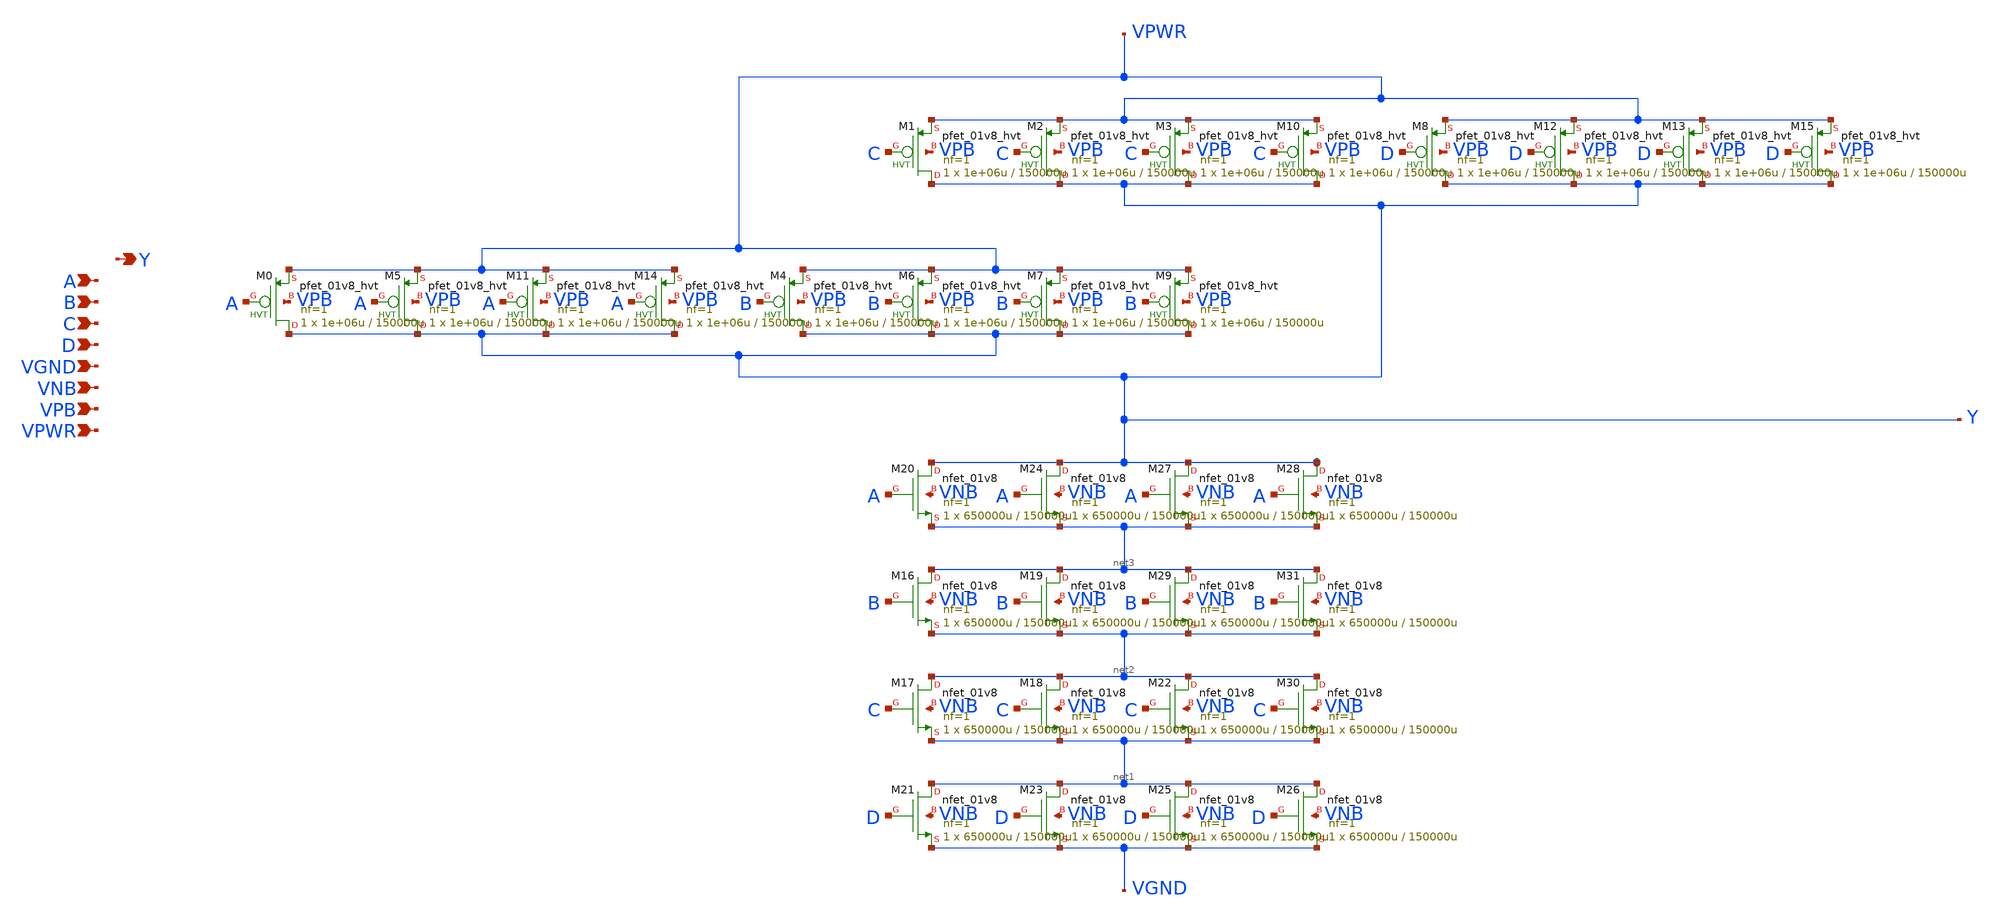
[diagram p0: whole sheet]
** sch_path: schematics/nand4/sky130_fd_sc_hd__nand4_4.sch
**.subckt sky130_fd_sc_hd__nand4_4 A B C D VGND VNB VPB VPWR Y
*.ipin A
*.ipin B
*.ipin C
*.ipin D
*.ipin VGND
*.ipin VNB
*.ipin VPB
*.ipin VPWR
*.opin Y
XM0 Y A VPWR VPB sky130_fd_pr__pfet_01v8_hvt L=150000u W=1e+06u nf=1 ad='int((1 + 1)/2) * 1e+06u / 1 * 0.29'
+ as='int((1 + 2)/2) * 1e+06u / 1 * 0.29' pd='2*int((1 + 1)/2) * (1e+06u / 1 + 0.29)' ps='2*int((1 + 2)/2) * (1e+06u / 1 + 0.29)'
+ nrd='0.29 / 1e+06u ' nrs='0.29 / 1e+06u ' sa=0 sb=0 sd=0 mult=1 m=1
XM1 Y C VPWR VPB sky130_fd_pr__pfet_01v8_hvt L=150000u W=1e+06u nf=1 ad='int((1 + 1)/2) * 1e+06u / 1 * 0.29'
+ as='int((1 + 2)/2) * 1e+06u / 1 * 0.29' pd='2*int((1 + 1)/2) * (1e+06u / 1 + 0.29)' ps='2*int((1 + 2)/2) * (1e+06u / 1 + 0.29)'
+ nrd='0.29 / 1e+06u ' nrs='0.29 / 1e+06u ' sa=0 sb=0 sd=0 mult=1 m=1
XM2 Y C VPWR VPB sky130_fd_pr__pfet_01v8_hvt L=150000u W=1e+06u nf=1 ad='int((1 + 1)/2) * 1e+06u / 1 * 0.29'
+ as='int((1 + 2)/2) * 1e+06u / 1 * 0.29' pd='2*int((1 + 1)/2) * (1e+06u / 1 + 0.29)' ps='2*int((1 + 2)/2) * (1e+06u / 1 + 0.29)'
+ nrd='0.29 / 1e+06u ' nrs='0.29 / 1e+06u ' sa=0 sb=0 sd=0 mult=1 m=1
XM3 Y C VPWR VPB sky130_fd_pr__pfet_01v8_hvt L=150000u W=1e+06u nf=1 ad='int((1 + 1)/2) * 1e+06u / 1 * 0.29'
+ as='int((1 + 2)/2) * 1e+06u / 1 * 0.29' pd='2*int((1 + 1)/2) * (1e+06u / 1 + 0.29)' ps='2*int((1 + 2)/2) * (1e+06u / 1 + 0.29)'
+ nrd='0.29 / 1e+06u ' nrs='0.29 / 1e+06u ' sa=0 sb=0 sd=0 mult=1 m=1
XM4 Y B VPWR VPB sky130_fd_pr__pfet_01v8_hvt L=150000u W=1e+06u nf=1 ad='int((1 + 1)/2) * 1e+06u / 1 * 0.29'
+ as='int((1 + 2)/2) * 1e+06u / 1 * 0.29' pd='2*int((1 + 1)/2) * (1e+06u / 1 + 0.29)' ps='2*int((1 + 2)/2) * (1e+06u / 1 + 0.29)'
+ nrd='0.29 / 1e+06u ' nrs='0.29 / 1e+06u ' sa=0 sb=0 sd=0 mult=1 m=1
XM5 Y A VPWR VPB sky130_fd_pr__pfet_01v8_hvt L=150000u W=1e+06u nf=1 ad='int((1 + 1)/2) * 1e+06u / 1 * 0.29'
+ as='int((1 + 2)/2) * 1e+06u / 1 * 0.29' pd='2*int((1 + 1)/2) * (1e+06u / 1 + 0.29)' ps='2*int((1 + 2)/2) * (1e+06u / 1 + 0.29)'
+ nrd='0.29 / 1e+06u ' nrs='0.29 / 1e+06u ' sa=0 sb=0 sd=0 mult=1 m=1
XM6 Y B VPWR VPB sky130_fd_pr__pfet_01v8_hvt L=150000u W=1e+06u nf=1 ad='int((1 + 1)/2) * 1e+06u / 1 * 0.29'
+ as='int((1 + 2)/2) * 1e+06u / 1 * 0.29' pd='2*int((1 + 1)/2) * (1e+06u / 1 + 0.29)' ps='2*int((1 + 2)/2) * (1e+06u / 1 + 0.29)'
+ nrd='0.29 / 1e+06u ' nrs='0.29 / 1e+06u ' sa=0 sb=0 sd=0 mult=1 m=1
XM7 Y B VPWR VPB sky130_fd_pr__pfet_01v8_hvt L=150000u W=1e+06u nf=1 ad='int((1 + 1)/2) * 1e+06u / 1 * 0.29'
+ as='int((1 + 2)/2) * 1e+06u / 1 * 0.29' pd='2*int((1 + 1)/2) * (1e+06u / 1 + 0.29)' ps='2*int((1 + 2)/2) * (1e+06u / 1 + 0.29)'
+ nrd='0.29 / 1e+06u ' nrs='0.29 / 1e+06u ' sa=0 sb=0 sd=0 mult=1 m=1
XM8 Y D VPWR VPB sky130_fd_pr__pfet_01v8_hvt L=150000u W=1e+06u nf=1 ad='int((1 + 1)/2) * 1e+06u / 1 * 0.29'
+ as='int((1 + 2)/2) * 1e+06u / 1 * 0.29' pd='2*int((1 + 1)/2) * (1e+06u / 1 + 0.29)' ps='2*int((1 + 2)/2) * (1e+06u / 1 + 0.29)'
+ nrd='0.29 / 1e+06u ' nrs='0.29 / 1e+06u ' sa=0 sb=0 sd=0 mult=1 m=1
XM9 Y B VPWR VPB sky130_fd_pr__pfet_01v8_hvt L=150000u W=1e+06u nf=1 ad='int((1 + 1)/2) * 1e+06u / 1 * 0.29'
+ as='int((1 + 2)/2) * 1e+06u / 1 * 0.29' pd='2*int((1 + 1)/2) * (1e+06u / 1 + 0.29)' ps='2*int((1 + 2)/2) * (1e+06u / 1 + 0.29)'
+ nrd='0.29 / 1e+06u ' nrs='0.29 / 1e+06u ' sa=0 sb=0 sd=0 mult=1 m=1
XM10 Y C VPWR VPB sky130_fd_pr__pfet_01v8_hvt L=150000u W=1e+06u nf=1 ad='int((1 + 1)/2) * 1e+06u / 1 * 0.29'
+ as='int((1 + 2)/2) * 1e+06u / 1 * 0.29' pd='2*int((1 + 1)/2) * (1e+06u / 1 + 0.29)' ps='2*int((1 + 2)/2) * (1e+06u / 1 + 0.29)'
+ nrd='0.29 / 1e+06u ' nrs='0.29 / 1e+06u ' sa=0 sb=0 sd=0 mult=1 m=1
XM11 Y A VPWR VPB sky130_fd_pr__pfet_01v8_hvt L=150000u W=1e+06u nf=1 ad='int((1 + 1)/2) * 1e+06u / 1 * 0.29'
+ as='int((1 + 2)/2) * 1e+06u / 1 * 0.29' pd='2*int((1 + 1)/2) * (1e+06u / 1 + 0.29)' ps='2*int((1 + 2)/2) * (1e+06u / 1 + 0.29)'
+ nrd='0.29 / 1e+06u ' nrs='0.29 / 1e+06u ' sa=0 sb=0 sd=0 mult=1 m=1
XM12 Y D VPWR VPB sky130_fd_pr__pfet_01v8_hvt L=150000u W=1e+06u nf=1 ad='int((1 + 1)/2) * 1e+06u / 1 * 0.29'
+ as='int((1 + 2)/2) * 1e+06u / 1 * 0.29' pd='2*int((1 + 1)/2) * (1e+06u / 1 + 0.29)' ps='2*int((1 + 2)/2) * (1e+06u / 1 + 0.29)'
+ nrd='0.29 / 1e+06u ' nrs='0.29 / 1e+06u ' sa=0 sb=0 sd=0 mult=1 m=1
XM13 Y D VPWR VPB sky130_fd_pr__pfet_01v8_hvt L=150000u W=1e+06u nf=1 ad='int((1 + 1)/2) * 1e+06u / 1 * 0.29'
+ as='int((1 + 2)/2) * 1e+06u / 1 * 0.29' pd='2*int((1 + 1)/2) * (1e+06u / 1 + 0.29)' ps='2*int((1 + 2)/2) * (1e+06u / 1 + 0.29)'
+ nrd='0.29 / 1e+06u ' nrs='0.29 / 1e+06u ' sa=0 sb=0 sd=0 mult=1 m=1
XM14 Y A VPWR VPB sky130_fd_pr__pfet_01v8_hvt L=150000u W=1e+06u nf=1 ad='int((1 + 1)/2) * 1e+06u / 1 * 0.29'
+ as='int((1 + 2)/2) * 1e+06u / 1 * 0.29' pd='2*int((1 + 1)/2) * (1e+06u / 1 + 0.29)' ps='2*int((1 + 2)/2) * (1e+06u / 1 + 0.29)'
+ nrd='0.29 / 1e+06u ' nrs='0.29 / 1e+06u ' sa=0 sb=0 sd=0 mult=1 m=1
XM15 Y D VPWR VPB sky130_fd_pr__pfet_01v8_hvt L=150000u W=1e+06u nf=1 ad='int((1 + 1)/2) * 1e+06u / 1 * 0.29'
+ as='int((1 + 2)/2) * 1e+06u / 1 * 0.29' pd='2*int((1 + 1)/2) * (1e+06u / 1 + 0.29)' ps='2*int((1 + 2)/2) * (1e+06u / 1 + 0.29)'
+ nrd='0.29 / 1e+06u ' nrs='0.29 / 1e+06u ' sa=0 sb=0 sd=0 mult=1 m=1
XM16 net3 B net2 VNB sky130_fd_pr__nfet_01v8 L=150000u W=650000u nf=1 ad='int((1 + 1)/2) * 650000u / 1 * 0.29'
+ as='int((1 + 2)/2) * 650000u / 1 * 0.29' pd='2*int((1 + 1)/2) * (650000u / 1 + 0.29)' ps='2*int((1 + 2)/2) * (650000u / 1 + 0.29)'
+ nrd='0.29 / 650000u ' nrs='0.29 / 650000u ' sa=0 sb=0 sd=0 mult=1 m=1
XM17 net2 C net1 VNB sky130_fd_pr__nfet_01v8 L=150000u W=650000u nf=1 ad='int((1 + 1)/2) * 650000u / 1 * 0.29'
+ as='int((1 + 2)/2) * 650000u / 1 * 0.29' pd='2*int((1 + 1)/2) * (650000u / 1 + 0.29)' ps='2*int((1 + 2)/2) * (650000u / 1 + 0.29)'
+ nrd='0.29 / 650000u ' nrs='0.29 / 650000u ' sa=0 sb=0 sd=0 mult=1 m=1
XM18 net2 C net1 VNB sky130_fd_pr__nfet_01v8 L=150000u W=650000u nf=1 ad='int((1 + 1)/2) * 650000u / 1 * 0.29'
+ as='int((1 + 2)/2) * 650000u / 1 * 0.29' pd='2*int((1 + 1)/2) * (650000u / 1 + 0.29)' ps='2*int((1 + 2)/2) * (650000u / 1 + 0.29)'
+ nrd='0.29 / 650000u ' nrs='0.29 / 650000u ' sa=0 sb=0 sd=0 mult=1 m=1
XM19 net3 B net2 VNB sky130_fd_pr__nfet_01v8 L=150000u W=650000u nf=1 ad='int((1 + 1)/2) * 650000u / 1 * 0.29'
+ as='int((1 + 2)/2) * 650000u / 1 * 0.29' pd='2*int((1 + 1)/2) * (650000u / 1 + 0.29)' ps='2*int((1 + 2)/2) * (650000u / 1 + 0.29)'
+ nrd='0.29 / 650000u ' nrs='0.29 / 650000u ' sa=0 sb=0 sd=0 mult=1 m=1
XM20 Y A net3 VNB sky130_fd_pr__nfet_01v8 L=150000u W=650000u nf=1 ad='int((1 + 1)/2) * 650000u / 1 * 0.29'
+ as='int((1 + 2)/2) * 650000u / 1 * 0.29' pd='2*int((1 + 1)/2) * (650000u / 1 + 0.29)' ps='2*int((1 + 2)/2) * (650000u / 1 + 0.29)'
+ nrd='0.29 / 650000u ' nrs='0.29 / 650000u ' sa=0 sb=0 sd=0 mult=1 m=1
XM21 net1 D VGND VNB sky130_fd_pr__nfet_01v8 L=150000u W=650000u nf=1 ad='int((1 + 1)/2) * 650000u / 1 * 0.29'
+ as='int((1 + 2)/2) * 650000u / 1 * 0.29' pd='2*int((1 + 1)/2) * (650000u / 1 + 0.29)' ps='2*int((1 + 2)/2) * (650000u / 1 + 0.29)'
+ nrd='0.29 / 650000u ' nrs='0.29 / 650000u ' sa=0 sb=0 sd=0 mult=1 m=1
XM22 net2 C net1 VNB sky130_fd_pr__nfet_01v8 L=150000u W=650000u nf=1 ad='int((1 + 1)/2) * 650000u / 1 * 0.29'
+ as='int((1 + 2)/2) * 650000u / 1 * 0.29' pd='2*int((1 + 1)/2) * (650000u / 1 + 0.29)' ps='2*int((1 + 2)/2) * (650000u / 1 + 0.29)'
+ nrd='0.29 / 650000u ' nrs='0.29 / 650000u ' sa=0 sb=0 sd=0 mult=1 m=1
XM23 net1 D VGND VNB sky130_fd_pr__nfet_01v8 L=150000u W=650000u nf=1 ad='int((1 + 1)/2) * 650000u / 1 * 0.29'
+ as='int((1 + 2)/2) * 650000u / 1 * 0.29' pd='2*int((1 + 1)/2) * (650000u / 1 + 0.29)' ps='2*int((1 + 2)/2) * (650000u / 1 + 0.29)'
+ nrd='0.29 / 650000u ' nrs='0.29 / 650000u ' sa=0 sb=0 sd=0 mult=1 m=1
XM24 Y A net3 VNB sky130_fd_pr__nfet_01v8 L=150000u W=650000u nf=1 ad='int((1 + 1)/2) * 650000u / 1 * 0.29'
+ as='int((1 + 2)/2) * 650000u / 1 * 0.29' pd='2*int((1 + 1)/2) * (650000u / 1 + 0.29)' ps='2*int((1 + 2)/2) * (650000u / 1 + 0.29)'
+ nrd='0.29 / 650000u ' nrs='0.29 / 650000u ' sa=0 sb=0 sd=0 mult=1 m=1
XM25 net1 D VGND VNB sky130_fd_pr__nfet_01v8 L=150000u W=650000u nf=1 ad='int((1 + 1)/2) * 650000u / 1 * 0.29'
+ as='int((1 + 2)/2) * 650000u / 1 * 0.29' pd='2*int((1 + 1)/2) * (650000u / 1 + 0.29)' ps='2*int((1 + 2)/2) * (650000u / 1 + 0.29)'
+ nrd='0.29 / 650000u ' nrs='0.29 / 650000u ' sa=0 sb=0 sd=0 mult=1 m=1
XM26 net1 D VGND VNB sky130_fd_pr__nfet_01v8 L=150000u W=650000u nf=1 ad='int((1 + 1)/2) * 650000u / 1 * 0.29'
+ as='int((1 + 2)/2) * 650000u / 1 * 0.29' pd='2*int((1 + 1)/2) * (650000u / 1 + 0.29)' ps='2*int((1 + 2)/2) * (650000u / 1 + 0.29)'
+ nrd='0.29 / 650000u ' nrs='0.29 / 650000u ' sa=0 sb=0 sd=0 mult=1 m=1
XM27 Y A net3 VNB sky130_fd_pr__nfet_01v8 L=150000u W=650000u nf=1 ad='int((1 + 1)/2) * 650000u / 1 * 0.29'
+ as='int((1 + 2)/2) * 650000u / 1 * 0.29' pd='2*int((1 + 1)/2) * (650000u / 1 + 0.29)' ps='2*int((1 + 2)/2) * (650000u / 1 + 0.29)'
+ nrd='0.29 / 650000u ' nrs='0.29 / 650000u ' sa=0 sb=0 sd=0 mult=1 m=1
XM28 Y A net3 VNB sky130_fd_pr__nfet_01v8 L=150000u W=650000u nf=1 ad='int((1 + 1)/2) * 650000u / 1 * 0.29'
+ as='int((1 + 2)/2) * 650000u / 1 * 0.29' pd='2*int((1 + 1)/2) * (650000u / 1 + 0.29)' ps='2*int((1 + 2)/2) * (650000u / 1 + 0.29)'
+ nrd='0.29 / 650000u ' nrs='0.29 / 650000u ' sa=0 sb=0 sd=0 mult=1 m=1
XM29 net3 B net2 VNB sky130_fd_pr__nfet_01v8 L=150000u W=650000u nf=1 ad='int((1 + 1)/2) * 650000u / 1 * 0.29'
+ as='int((1 + 2)/2) * 650000u / 1 * 0.29' pd='2*int((1 + 1)/2) * (650000u / 1 + 0.29)' ps='2*int((1 + 2)/2) * (650000u / 1 + 0.29)'
+ nrd='0.29 / 650000u ' nrs='0.29 / 650000u ' sa=0 sb=0 sd=0 mult=1 m=1
XM30 net2 C net1 VNB sky130_fd_pr__nfet_01v8 L=150000u W=650000u nf=1 ad='int((1 + 1)/2) * 650000u / 1 * 0.29'
+ as='int((1 + 2)/2) * 650000u / 1 * 0.29' pd='2*int((1 + 1)/2) * (650000u / 1 + 0.29)' ps='2*int((1 + 2)/2) * (650000u / 1 + 0.29)'
+ nrd='0.29 / 650000u ' nrs='0.29 / 650000u ' sa=0 sb=0 sd=0 mult=1 m=1
XM31 net3 B net2 VNB sky130_fd_pr__nfet_01v8 L=150000u W=650000u nf=1 ad='int((1 + 1)/2) * 650000u / 1 * 0.29'
+ as='int((1 + 2)/2) * 650000u / 1 * 0.29' pd='2*int((1 + 1)/2) * (650000u / 1 + 0.29)' ps='2*int((1 + 2)/2) * (650000u / 1 + 0.29)'
+ nrd='0.29 / 650000u ' nrs='0.29 / 650000u ' sa=0 sb=0 sd=0 mult=1 m=1
**.ends
.end
